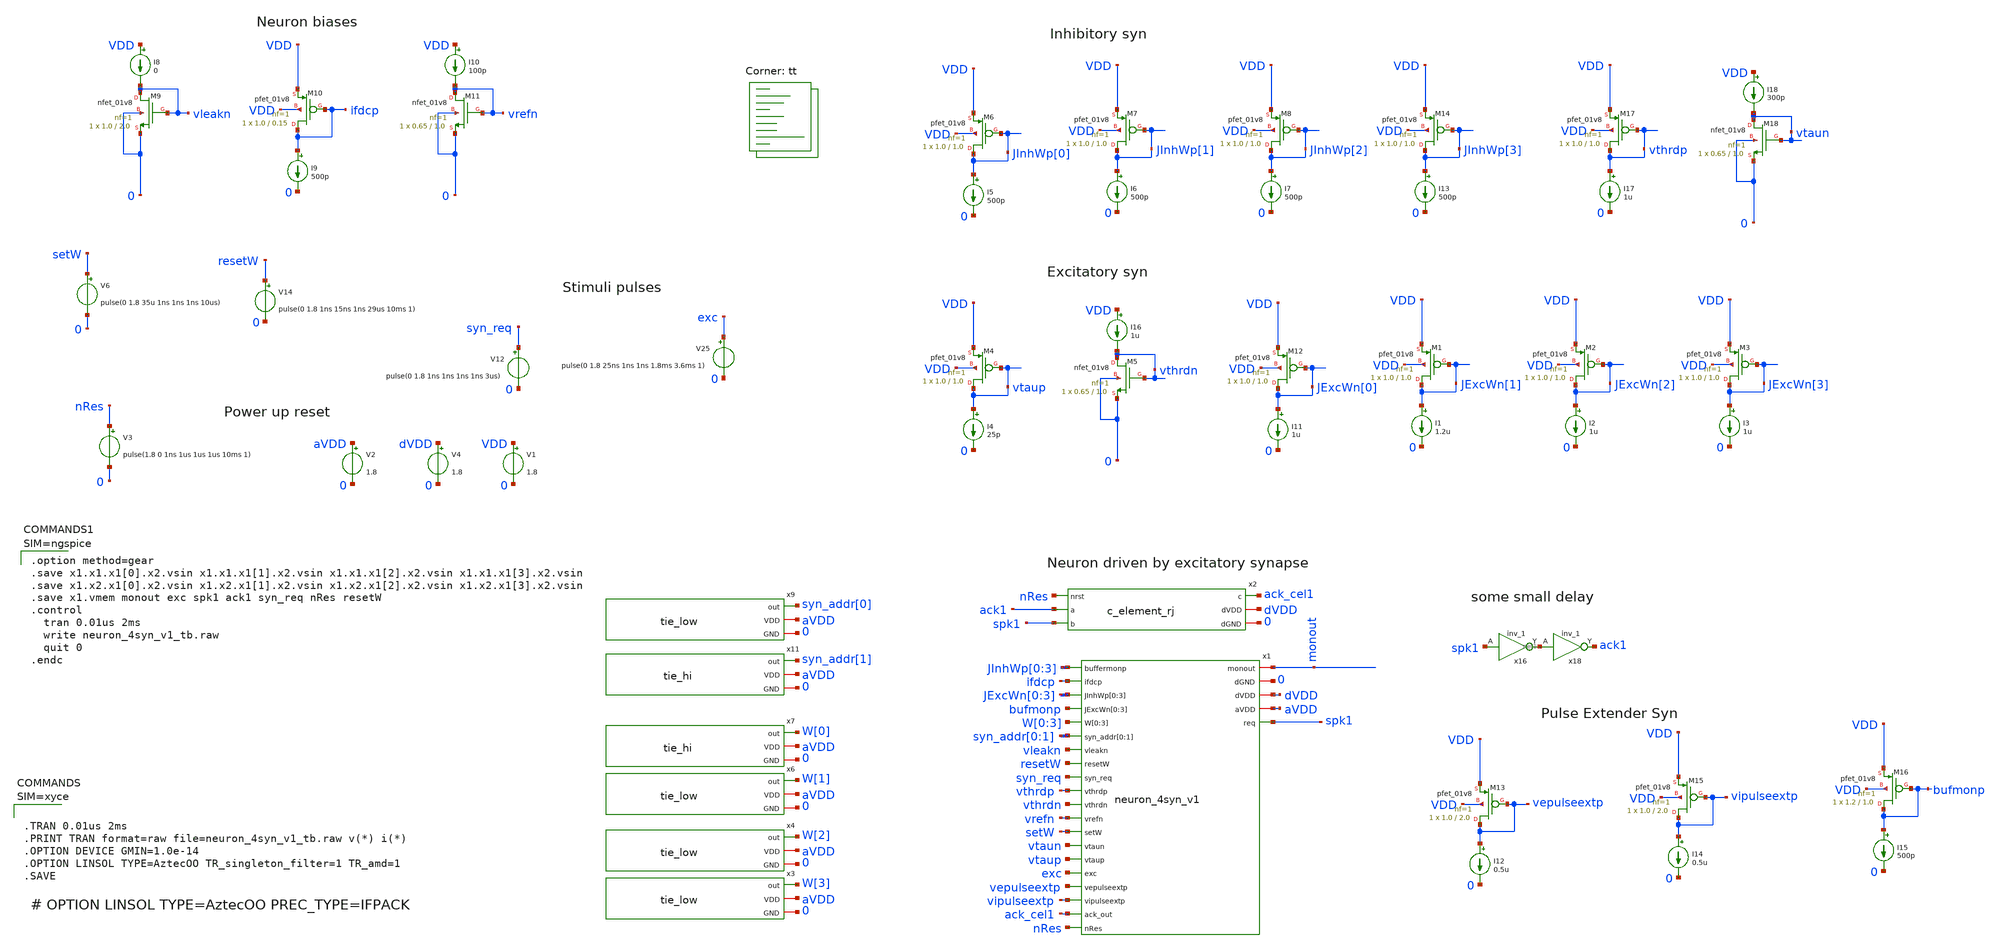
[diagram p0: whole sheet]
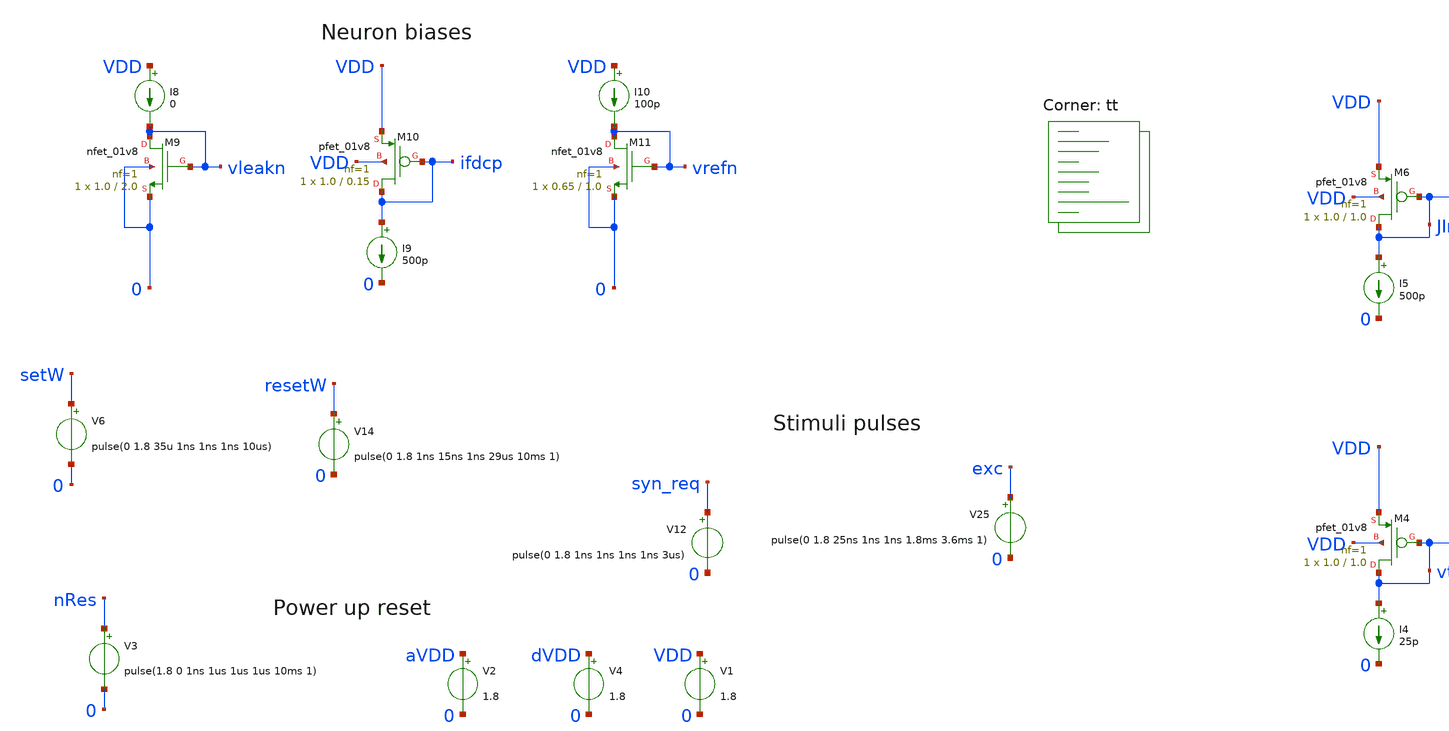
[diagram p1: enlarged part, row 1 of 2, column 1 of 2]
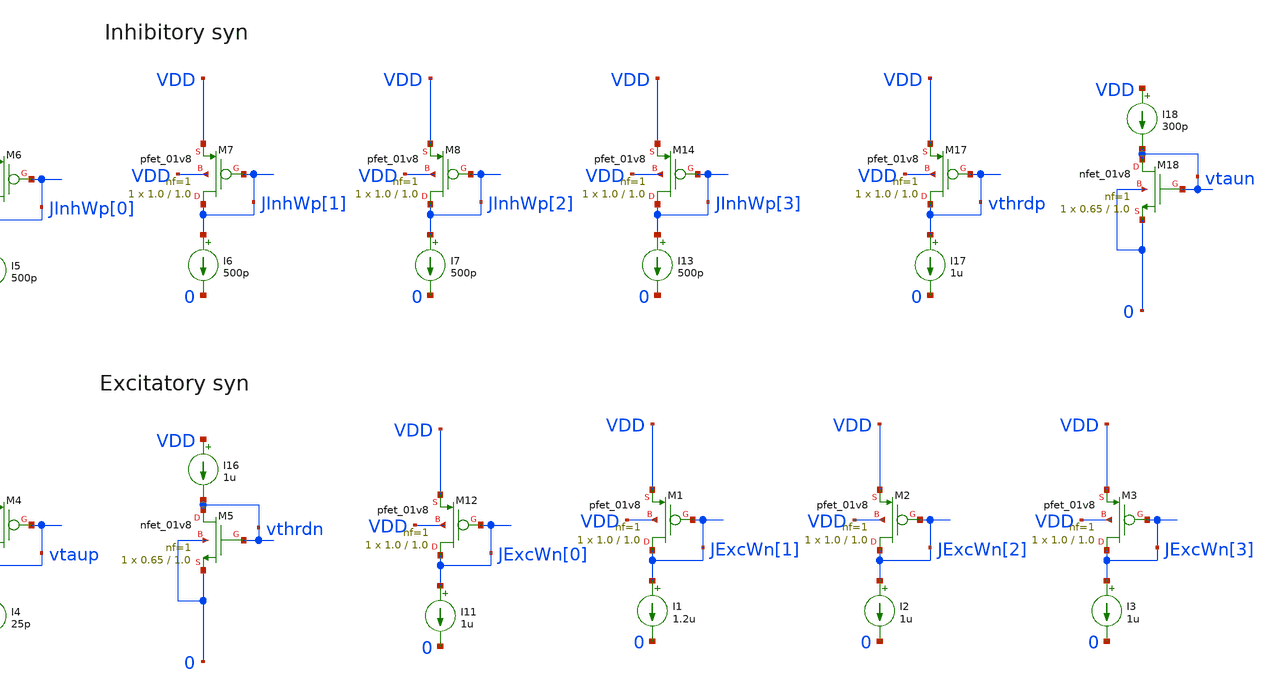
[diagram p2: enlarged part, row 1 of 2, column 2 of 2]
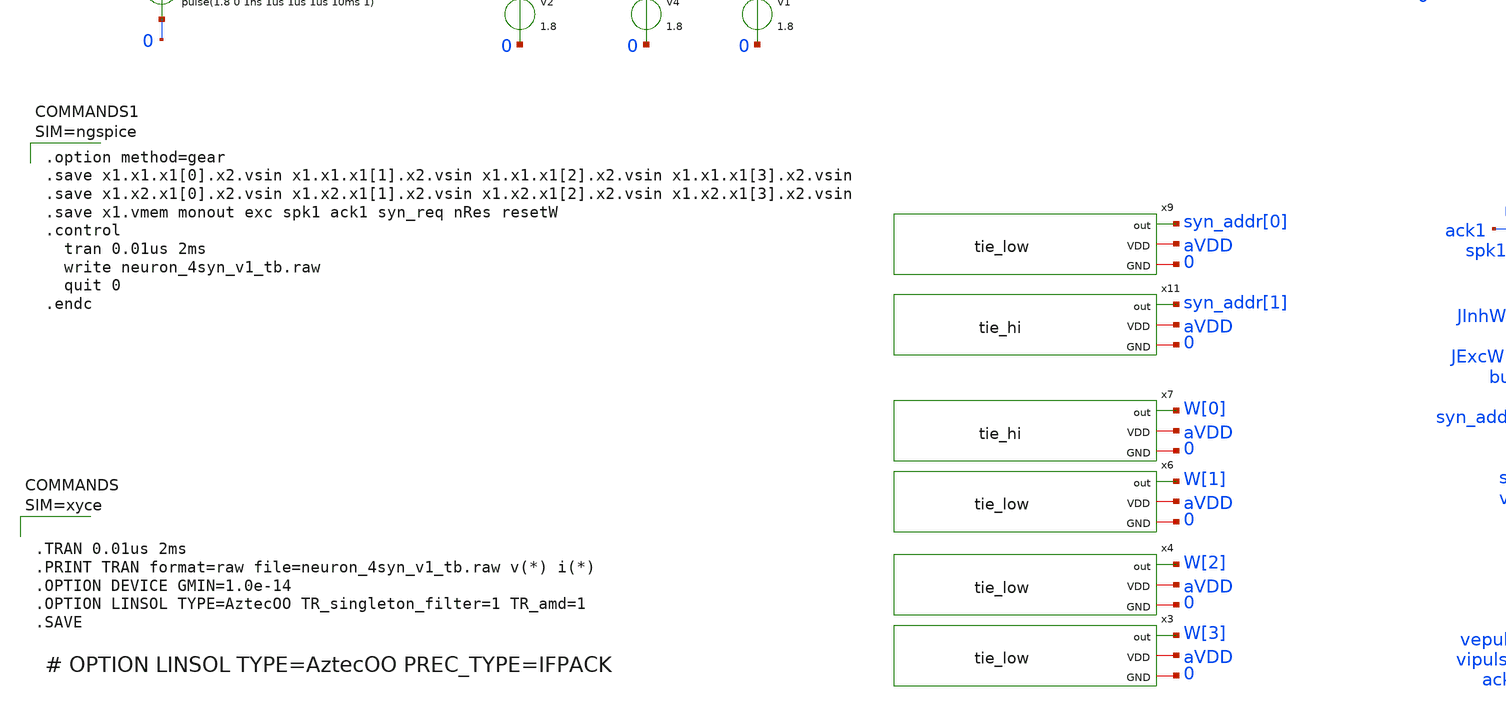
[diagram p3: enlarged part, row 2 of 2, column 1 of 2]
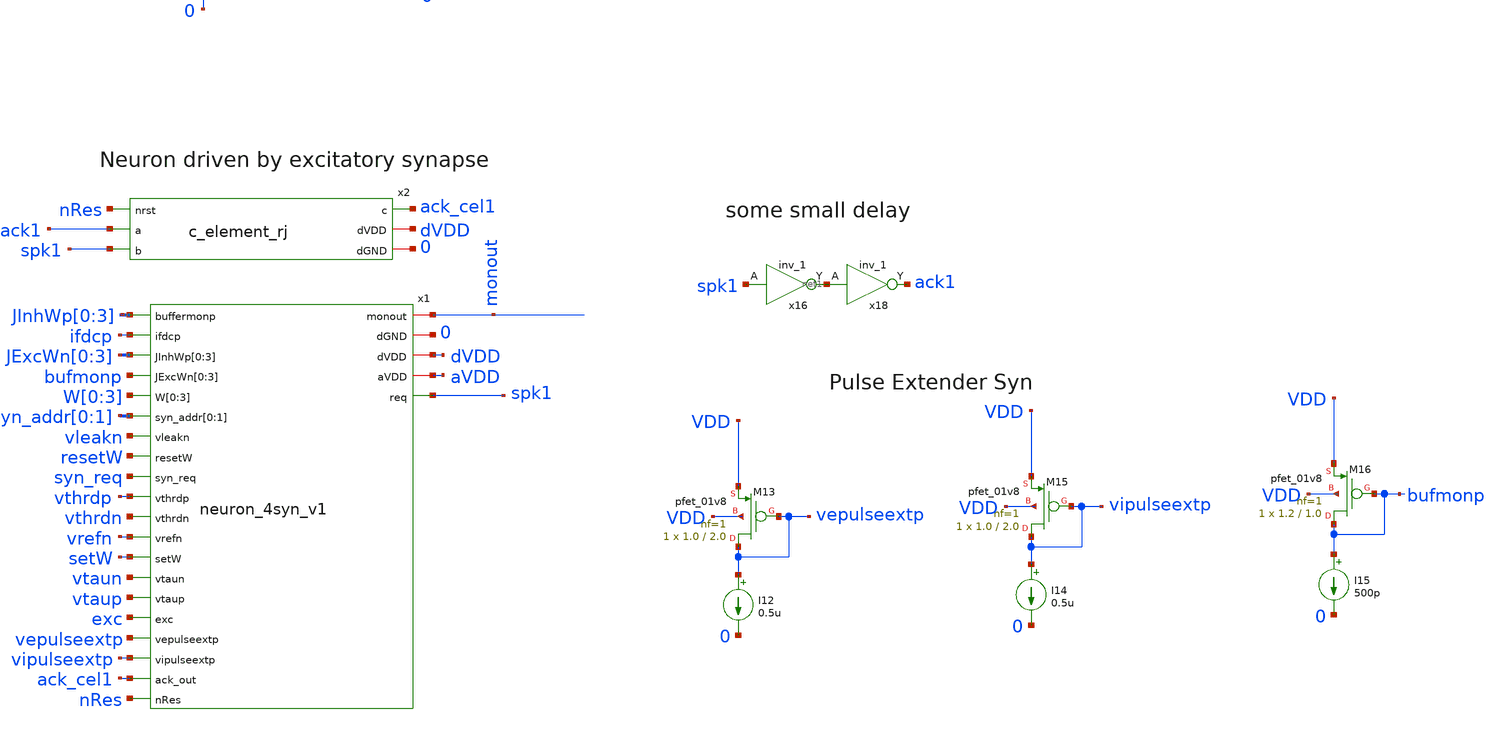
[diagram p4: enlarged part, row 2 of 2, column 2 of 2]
** sch_path: design/xschem/neuron_4syn_v1_tb.sch
**.subckt neuron_4syn_v1_tb
V2 aVDD 0 1.8
V12 syn_req 0 pulse(0 1.8 1ns 1ns 1ns 1ns 3us)
x2 nRes ack1 spk1 ack_cel1 dVDD 0 c_element_rj
x6 W[1] aVDD 0 tie_low
x7 W[0] aVDD 0 tie_hi
x9 syn_addr[0] aVDD 0 tie_low
x11 syn_addr[1] aVDD 0 tie_hi
V25 exc 0 pulse(0 1.8 25ns 1ns 1ns 1.8ms 3.6ms 1)
x16 spk1 0 0 dVDD dVDD net1 sky130_fd_sc_hd__inv_1
x18 net1 0 0 dVDD dVDD ack1 sky130_fd_sc_hd__inv_1
V4 dVDD 0 1.8
x1 JInhWp[0] ifdcp JExcWn[0] JExcWn[1] JExcWn[2] JExcWn[3] bufmonp bufmonp bufmonp bufmonp W[0] W[1]
+ W[2] W[3] syn_addr[0] syn_addr[1] vleakn monout resetW syn_req vthrdp vthrdn vrefn setW vtaun vtaup exc
+ vepulseextp vipulseextp 0 dVDD aVDD ack_cel1 spk1 nRes neuron_4syn_v1
V1 VDD 0 1.8
I8 VDD vleakn 0
XM9 vleakn vleakn 0 0 sky130_fd_pr__nfet_01v8 L=2.0 W=1.0 nf=1 ad='int((nf+1)/2) * W/nf * 0.29' as='int((nf+2)/2) * W/nf * 0.29'
+ pd='2*int((nf+1)/2) * (W/nf + 0.29)' ps='2*int((nf+2)/2) * (W/nf + 0.29)' nrd='0.29 / W' nrs='0.29 / W'
+ sa=0 sb=0 sd=0 mult=1 m=1
XM10 ifdcp ifdcp VDD VDD sky130_fd_pr__pfet_01v8 L=0.15 W=1.0 nf=1 ad='int((nf+1)/2) * W/nf * 0.29' as='int((nf+2)/2) * W/nf * 0.29'
+ pd='2*int((nf+1)/2) * (W/nf + 0.29)' ps='2*int((nf+2)/2) * (W/nf + 0.29)' nrd='0.29 / W' nrs='0.29 / W'
+ sa=0 sb=0 sd=0 mult=1 m=1
I9 ifdcp 0 500p
I10 VDD vrefn 100p
XM11 vrefn vrefn 0 0 sky130_fd_pr__nfet_01v8 L=1.0 W=0.65 nf=1 ad='int((nf+1)/2) * W/nf * 0.29' as='int((nf+2)/2) * W/nf * 0.29'
+ pd='2*int((nf+1)/2) * (W/nf + 0.29)' ps='2*int((nf+2)/2) * (W/nf + 0.29)' nrd='0.29 / W' nrs='0.29 / W'
+ sa=0 sb=0 sd=0 mult=1 m=1
XM13 vepulseextp vepulseextp VDD VDD sky130_fd_pr__pfet_01v8 L=2.0 W=1.0 nf=1 ad='int((nf+1)/2) * W/nf * 0.29'
+ as='int((nf+2)/2) * W/nf * 0.29' pd='2*int((nf+1)/2) * (W/nf + 0.29)' ps='2*int((nf+2)/2) * (W/nf + 0.29)'
+ nrd='0.29 / W' nrs='0.29 / W' sa=0 sb=0 sd=0 mult=1 m=1
I12 vepulseextp 0 0.5u
XM15 vipulseextp vipulseextp VDD VDD sky130_fd_pr__pfet_01v8 L=2.0 W=1.0 nf=1 ad='int((nf+1)/2) * W/nf * 0.29'
+ as='int((nf+2)/2) * W/nf * 0.29' pd='2*int((nf+1)/2) * (W/nf + 0.29)' ps='2*int((nf+2)/2) * (W/nf + 0.29)'
+ nrd='0.29 / W' nrs='0.29 / W' sa=0 sb=0 sd=0 mult=1 m=1
I14 vipulseextp 0 0.5u
XM16 bufmonp bufmonp VDD VDD sky130_fd_pr__pfet_01v8 L=1.0 W=1.2 nf=1 ad='int((nf+1)/2) * W/nf * 0.29'
+ as='int((nf+2)/2) * W/nf * 0.29' pd='2*int((nf+1)/2) * (W/nf + 0.29)' ps='2*int((nf+2)/2) * (W/nf + 0.29)'
+ nrd='0.29 / W' nrs='0.29 / W' sa=0 sb=0 sd=0 mult=1 m=1
I15 bufmonp 0 500p
x4 W[2] aVDD 0 tie_low
x3 W[3] aVDD 0 tie_low
XM12 JExcWn[0] JExcWn[0] VDD VDD sky130_fd_pr__pfet_01v8 L=1.0 W=1.0 nf=1 ad='int((nf+1)/2) * W/nf * 0.29'
+ as='int((nf+2)/2) * W/nf * 0.29' pd='2*int((nf+1)/2) * (W/nf + 0.29)' ps='2*int((nf+2)/2) * (W/nf + 0.29)'
+ nrd='0.29 / W' nrs='0.29 / W' sa=0 sb=0 sd=0 mult=1 m=1
I11 JExcWn[0] 0 1u
XM1 JExcWn[1] JExcWn[1] VDD VDD sky130_fd_pr__pfet_01v8 L=1.0 W=1.0 nf=1 ad='int((nf+1)/2) * W/nf * 0.29'
+ as='int((nf+2)/2) * W/nf * 0.29' pd='2*int((nf+1)/2) * (W/nf + 0.29)' ps='2*int((nf+2)/2) * (W/nf + 0.29)'
+ nrd='0.29 / W' nrs='0.29 / W' sa=0 sb=0 sd=0 mult=1 m=1
I1 JExcWn[1] 0 1.2u
XM2 JExcWn[2] JExcWn[2] VDD VDD sky130_fd_pr__pfet_01v8 L=1.0 W=1.0 nf=1 ad='int((nf+1)/2) * W/nf * 0.29'
+ as='int((nf+2)/2) * W/nf * 0.29' pd='2*int((nf+1)/2) * (W/nf + 0.29)' ps='2*int((nf+2)/2) * (W/nf + 0.29)'
+ nrd='0.29 / W' nrs='0.29 / W' sa=0 sb=0 sd=0 mult=1 m=1
I2 JExcWn[2] 0 1u
XM3 JExcWn[3] JExcWn[3] VDD VDD sky130_fd_pr__pfet_01v8 L=1.0 W=1.0 nf=1 ad='int((nf+1)/2) * W/nf * 0.29'
+ as='int((nf+2)/2) * W/nf * 0.29' pd='2*int((nf+1)/2) * (W/nf + 0.29)' ps='2*int((nf+2)/2) * (W/nf + 0.29)'
+ nrd='0.29 / W' nrs='0.29 / W' sa=0 sb=0 sd=0 mult=1 m=1
I3 JExcWn[3] 0 1u
XM4 vtaup vtaup VDD VDD sky130_fd_pr__pfet_01v8 L=1.0 W=1.0 nf=1 ad='int((nf+1)/2) * W/nf * 0.29' as='int((nf+2)/2) * W/nf * 0.29'
+ pd='2*int((nf+1)/2) * (W/nf + 0.29)' ps='2*int((nf+2)/2) * (W/nf + 0.29)' nrd='0.29 / W' nrs='0.29 / W'
+ sa=0 sb=0 sd=0 mult=1 m=1
I4 vtaup 0 25p
I16 VDD vthrdn 1u
XM5 vthrdn vthrdn 0 0 sky130_fd_pr__nfet_01v8 L=1.0 W=0.65 nf=1 ad='int((nf+1)/2) * W/nf * 0.29' as='int((nf+2)/2) * W/nf * 0.29'
+ pd='2*int((nf+1)/2) * (W/nf + 0.29)' ps='2*int((nf+2)/2) * (W/nf + 0.29)' nrd='0.29 / W' nrs='0.29 / W'
+ sa=0 sb=0 sd=0 mult=1 m=1
XM6 JInhWp[0] JInhWp[0] VDD VDD sky130_fd_pr__pfet_01v8 L=1.0 W=1.0 nf=1 ad='int((nf+1)/2) * W/nf * 0.29'
+ as='int((nf+2)/2) * W/nf * 0.29' pd='2*int((nf+1)/2) * (W/nf + 0.29)' ps='2*int((nf+2)/2) * (W/nf + 0.29)'
+ nrd='0.29 / W' nrs='0.29 / W' sa=0 sb=0 sd=0 mult=1 m=1
I5 JInhWp[0] 0 500p
XM7 JInhWp[1] JInhWp[1] VDD VDD sky130_fd_pr__pfet_01v8 L=1.0 W=1.0 nf=1 ad='int((nf+1)/2) * W/nf * 0.29'
+ as='int((nf+2)/2) * W/nf * 0.29' pd='2*int((nf+1)/2) * (W/nf + 0.29)' ps='2*int((nf+2)/2) * (W/nf + 0.29)'
+ nrd='0.29 / W' nrs='0.29 / W' sa=0 sb=0 sd=0 mult=1 m=1
I6 JInhWp[1] 0 500p
XM8 JInhWp[2] JInhWp[2] VDD VDD sky130_fd_pr__pfet_01v8 L=1.0 W=1.0 nf=1 ad='int((nf+1)/2) * W/nf * 0.29'
+ as='int((nf+2)/2) * W/nf * 0.29' pd='2*int((nf+1)/2) * (W/nf + 0.29)' ps='2*int((nf+2)/2) * (W/nf + 0.29)'
+ nrd='0.29 / W' nrs='0.29 / W' sa=0 sb=0 sd=0 mult=1 m=1
I7 JInhWp[2] 0 500p
XM14 JInhWp[3] JInhWp[3] VDD VDD sky130_fd_pr__pfet_01v8 L=1.0 W=1.0 nf=1 ad='int((nf+1)/2) * W/nf * 0.29'
+ as='int((nf+2)/2) * W/nf * 0.29' pd='2*int((nf+1)/2) * (W/nf + 0.29)' ps='2*int((nf+2)/2) * (W/nf + 0.29)'
+ nrd='0.29 / W' nrs='0.29 / W' sa=0 sb=0 sd=0 mult=1 m=1
I13 JInhWp[3] 0 500p
XM17 vthrdp vthrdp VDD VDD sky130_fd_pr__pfet_01v8 L=1.0 W=1.0 nf=1 ad='int((nf+1)/2) * W/nf * 0.29'
+ as='int((nf+2)/2) * W/nf * 0.29' pd='2*int((nf+1)/2) * (W/nf + 0.29)' ps='2*int((nf+2)/2) * (W/nf + 0.29)'
+ nrd='0.29 / W' nrs='0.29 / W' sa=0 sb=0 sd=0 mult=1 m=1
I17 vthrdp 0 1u
I18 VDD vtaun 300p
XM18 vtaun vtaun 0 0 sky130_fd_pr__nfet_01v8 L=1.0 W=0.65 nf=1 ad='int((nf+1)/2) * W/nf * 0.29' as='int((nf+2)/2) * W/nf * 0.29'
+ pd='2*int((nf+1)/2) * (W/nf + 0.29)' ps='2*int((nf+2)/2) * (W/nf + 0.29)' nrd='0.29 / W' nrs='0.29 / W'
+ sa=0 sb=0 sd=0 mult=1 m=1
V3 nRes 0 pulse(1.8 0 1ns 1us 1us 1us 10ms 1)
V6 setW 0 pulse(0 1.8 35u 1ns 1ns 1ns 10us)
V14 resetW 0 pulse(0 1.8 1ns 15ns 1ns 29us 10ms 1)
**** begin user architecture code


* Standard cell simulation files
.include $::SKYWATER_STDCELLS/sky130_fd_sc_hd.spice


.lib $::SKYWATER_MODELS/sky130.lib.spice tt





.option method=gear
.save x1.x1.x1[0].x2.vsin x1.x1.x1[1].x2.vsin x1.x1.x1[2].x2.vsin x1.x1.x1[3].x2.vsin
.save x1.x2.x1[0].x2.vsin x1.x2.x1[1].x2.vsin x1.x2.x1[2].x2.vsin x1.x2.x1[3].x2.vsin
.save x1.vmem monout exc spk1 ack1 syn_req nRes resetW
.control
  tran 0.01us 2ms
  write neuron_4syn_v1_tb.raw
  quit 0
.endc


**** end user architecture code
**.ends
.end
